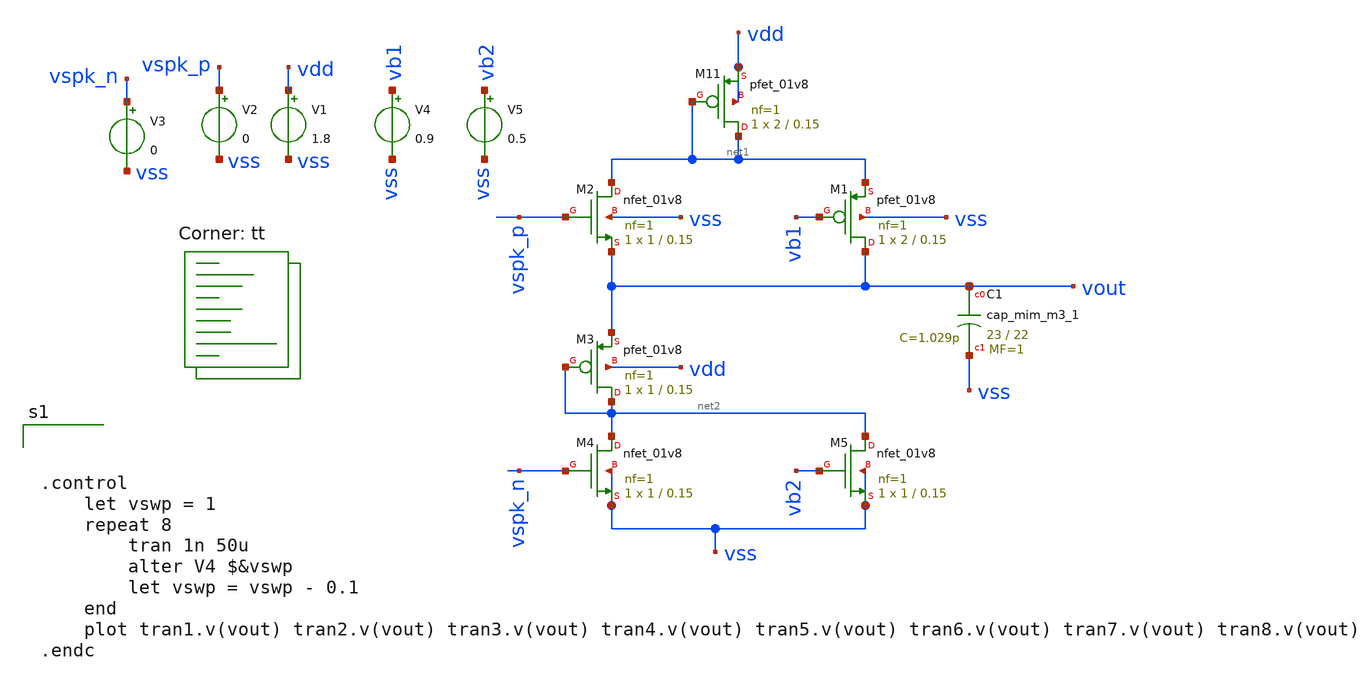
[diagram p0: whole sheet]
** sch_path: encoders/stepforward_int.sch
**.subckt stepforward_int
XM11 net1 net1 vdd vdd sky130_fd_pr__pfet_01v8 L=0.15 W=2 nf=1 ad='int((nf+1)/2) * W/nf * 0.29' as='int((nf+2)/2) * W/nf * 0.29'
+ pd='2*int((nf+1)/2) * (W/nf + 0.29)' ps='2*int((nf+2)/2) * (W/nf + 0.29)' nrd='0.29 / W' nrs='0.29 / W'
+ sa=0 sb=0 sd=0 mult=1 m=1
XC1 vout vss sky130_fd_pr__cap_mim_m3_1 W=23 L=22 MF=1 m=1
XM3 net2 net2 vout vdd sky130_fd_pr__pfet_01v8 L=0.15 W=1 nf=1 ad='int((nf+1)/2) * W/nf * 0.29' as='int((nf+2)/2) * W/nf * 0.29'
+ pd='2*int((nf+1)/2) * (W/nf + 0.29)' ps='2*int((nf+2)/2) * (W/nf + 0.29)' nrd='0.29 / W' nrs='0.29 / W'
+ sa=0 sb=0 sd=0 mult=1 m=1
XM4 net2 vspk_n vss vss sky130_fd_pr__nfet_01v8 L=0.15 W=1 nf=1 ad='int((1 + 1)/2) * 1 / 1 * 0.29' as='int((1 + 2)/2) * 1 / 1 * 0.29'
+ pd='2*int((1 + 1)/2) * (1 / 1 + 0.29)' ps='2*int((1 + 2)/2) * (1 / 1 + 0.29)' nrd='0.29 / 1 ' nrs='0.29 / 1 '
+ sa=0 sb=0 sd=0 mult=1 m=1
XM2 net1 vspk_p vout vss sky130_fd_pr__nfet_01v8 L=0.15 W=1 nf=1 ad='int((1 + 1)/2) * 1 / 1 * 0.29' as='int((1 + 2)/2) * 1 / 1 * 0.29'
+ pd='2*int((1 + 1)/2) * (1 / 1 + 0.29)' ps='2*int((1 + 2)/2) * (1 / 1 + 0.29)' nrd='0.29 / 1 ' nrs='0.29 / 1 '
+ sa=0 sb=0 sd=0 mult=1 m=1
XM5 net2 vb2 vss vss sky130_fd_pr__nfet_01v8 L=0.15 W=1 nf=1 ad='int((1 + 1)/2) * 1 / 1 * 0.29' as='int((1 + 2)/2) * 1 / 1 * 0.29'
+ pd='2*int((1 + 1)/2) * (1 / 1 + 0.29)' ps='2*int((1 + 2)/2) * (1 / 1 + 0.29)' nrd='0.29 / 1 ' nrs='0.29 / 1 '
+ sa=0 sb=0 sd=0 mult=1 m=1
V1 vdd vss 1.8
V2 vspk_p vss 0
V3 vspk_n vss 0
V4 vb1 vss 0.9
V5 vb2 vss 0.5
XM1 vout vb1 net1 vss sky130_fd_pr__pfet_01v8 L=0.15 W=2 nf=1 ad='int((nf+1)/2) * W/nf * 0.29' as='int((nf+2)/2) * W/nf * 0.29'
+ pd='2*int((nf+1)/2) * (W/nf + 0.29)' ps='2*int((nf+2)/2) * (W/nf + 0.29)' nrd='0.29 / W' nrs='0.29 / W'
+ sa=0 sb=0 sd=0 mult=1 m=1
**** begin user architecture code
.lib $::SKYWATER_MODELS/sky130.lib.spice tt



.control
	let vswp = 1
	repeat 8
		tran 1n 50u
		alter V4 $&vswp
		let vswp = vswp - 0.1
	end
	plot tran1.v(vout) tran2.v(vout) tran3.v(vout) tran4.v(vout) tran5.v(vout) tran6.v(vout)
+ tran7.v(vout) tran8.v(vout)
.endc



**** end user architecture code
**.ends
.end
